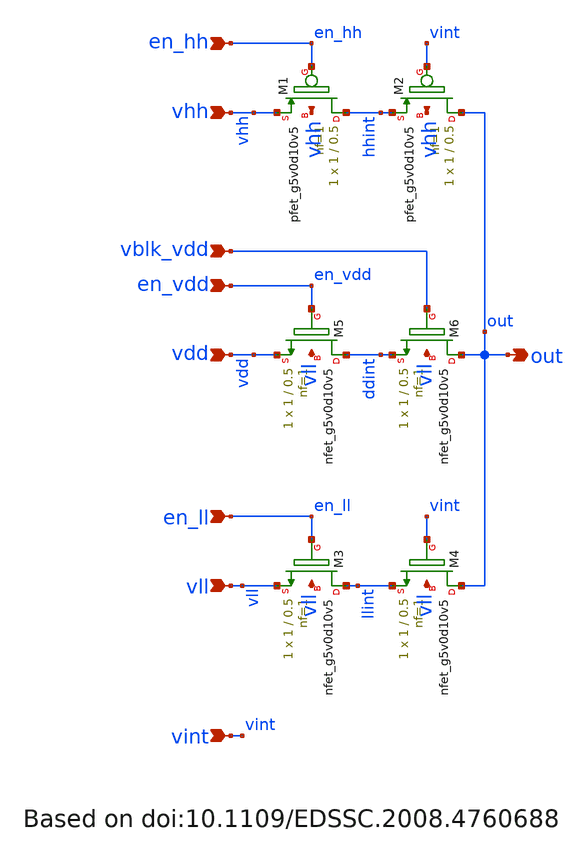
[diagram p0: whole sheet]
** sch_path: hvswitch_driver.sch
**.subckt hvswitch_driver vhh vll vint en_hh en_ll out vdd en_vdd vblk_vdd
*.ipin vhh
*.ipin vll
*.ipin vint
*.ipin en_hh
*.ipin en_ll
*.opin out
*.ipin vdd
*.ipin en_vdd
*.ipin vblk_vdd
XM3 llint en_ll vll vll sky130_fd_pr__nfet_g5v0d10v5 L=0.5 W=1 nf=1 ad='int((nf+1)/2) * W/nf * 0.29'
+ as='int((nf+2)/2) * W/nf * 0.29' pd='2*int((nf+1)/2) * (W/nf + 0.29)' ps='2*int((nf+2)/2) * (W/nf + 0.29)'
+ nrd='0.29 / W' nrs='0.29 / W' sa=0 sb=0 sd=0 mult=1 m=1
XM1 hhint en_hh vhh vhh sky130_fd_pr__pfet_g5v0d10v5 L=0.5 W=1 nf=1 ad='int((nf+1)/2) * W/nf * 0.29'
+ as='int((nf+2)/2) * W/nf * 0.29' pd='2*int((nf+1)/2) * (W/nf + 0.29)' ps='2*int((nf+2)/2) * (W/nf + 0.29)'
+ nrd='0.29 / W' nrs='0.29 / W' sa=0 sb=0 sd=0 mult=1 m=1
XM2 out vint hhint vhh sky130_fd_pr__pfet_g5v0d10v5 L=0.5 W=1 nf=1 ad='int((nf+1)/2) * W/nf * 0.29' as='int((nf+2)/2) * W/nf * 0.29'
+ pd='2*int((nf+1)/2) * (W/nf + 0.29)' ps='2*int((nf+2)/2) * (W/nf + 0.29)' nrd='0.29 / W' nrs='0.29 / W'
+ sa=0 sb=0 sd=0 mult=1 m=1
XM4 out vint llint vll sky130_fd_pr__nfet_g5v0d10v5 L=0.5 W=1 nf=1 ad='int((nf+1)/2) * W/nf * 0.29' as='int((nf+2)/2) * W/nf * 0.29'
+ pd='2*int((nf+1)/2) * (W/nf + 0.29)' ps='2*int((nf+2)/2) * (W/nf + 0.29)' nrd='0.29 / W' nrs='0.29 / W'
+ sa=0 sb=0 sd=0 mult=1 m=1
XM5 ddint en_vdd vdd vll sky130_fd_pr__nfet_g5v0d10v5 L=0.5 W=1 nf=1 ad='int((nf+1)/2) * W/nf * 0.29'
+ as='int((nf+2)/2) * W/nf * 0.29' pd='2*int((nf+1)/2) * (W/nf + 0.29)' ps='2*int((nf+2)/2) * (W/nf + 0.29)'
+ nrd='0.29 / W' nrs='0.29 / W' sa=0 sb=0 sd=0 mult=1 m=1
XM6 out vblk_vdd ddint vll sky130_fd_pr__nfet_g5v0d10v5 L=0.5 W=1 nf=1 ad='int((nf+1)/2) * W/nf * 0.29'
+ as='int((nf+2)/2) * W/nf * 0.29' pd='2*int((nf+1)/2) * (W/nf + 0.29)' ps='2*int((nf+2)/2) * (W/nf + 0.29)'
+ nrd='0.29 / W' nrs='0.29 / W' sa=0 sb=0 sd=0 mult=1 m=1
**.ends
.end
